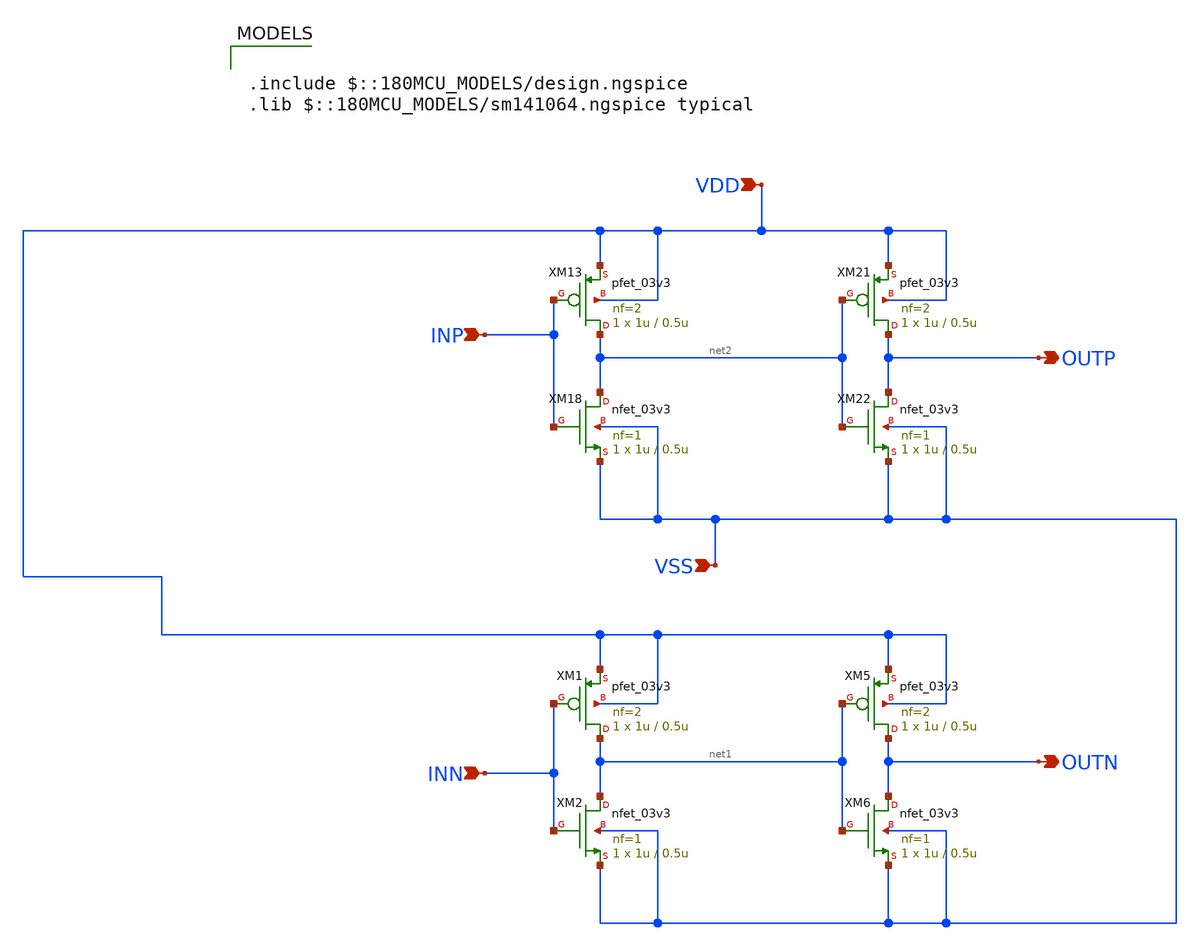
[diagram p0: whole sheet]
** sch_path: ISSCC26/submitted_notebooks/Low Mismatch 4 Channels Instrumentation Amplifier/Complementary Clock and Inverter/Schematic/clk_lpf_rev.sch
**.subckt clk_lpf_rev OUTP OUTN VDD VSS INP INN
*.opin OUTP
*.opin OUTN
*.ipin VDD
*.ipin VSS
*.ipin INP
*.ipin INN
XM1 net1 INN VDD VDD pfet_03v3 L=0.5u W=1u nf=2 ad='int((nf+1)/2) * W/nf * 0.18u' as='int((nf+2)/2) * W/nf * 0.18u'
+ pd='2*int((nf+1)/2) * (W/nf + 0.18u)' ps='2*int((nf+2)/2) * (W/nf + 0.18u)' nrd='0.18u / W' nrs='0.18u / W'
+ sa=0 sb=0 sd=0 m=1
XM2 net1 INN VSS VSS nfet_03v3 L=0.5u W=1u nf=1 ad='int((nf+1)/2) * W/nf * 0.18u' as='int((nf+2)/2) * W/nf * 0.18u'
+ pd='2*int((nf+1)/2) * (W/nf + 0.18u)' ps='2*int((nf+2)/2) * (W/nf + 0.18u)' nrd='0.18u / W' nrs='0.18u / W'
+ sa=0 sb=0 sd=0 m=1
XM5 OUTN net1 VDD VDD pfet_03v3 L=0.5u W=1u nf=2 ad='int((nf+1)/2) * W/nf * 0.18u' as='int((nf+2)/2) * W/nf * 0.18u'
+ pd='2*int((nf+1)/2) * (W/nf + 0.18u)' ps='2*int((nf+2)/2) * (W/nf + 0.18u)' nrd='0.18u / W' nrs='0.18u / W'
+ sa=0 sb=0 sd=0 m=1
XM6 OUTN net1 VSS VSS nfet_03v3 L=0.5u W=1u nf=1 ad='int((nf+1)/2) * W/nf * 0.18u' as='int((nf+2)/2) * W/nf * 0.18u'
+ pd='2*int((nf+1)/2) * (W/nf + 0.18u)' ps='2*int((nf+2)/2) * (W/nf + 0.18u)' nrd='0.18u / W' nrs='0.18u / W'
+ sa=0 sb=0 sd=0 m=1
XM13 net2 INP VDD VDD pfet_03v3 L=0.5u W=1u nf=2 ad='int((nf+1)/2) * W/nf * 0.18u' as='int((nf+2)/2) * W/nf * 0.18u'
+ pd='2*int((nf+1)/2) * (W/nf + 0.18u)' ps='2*int((nf+2)/2) * (W/nf + 0.18u)' nrd='0.18u / W' nrs='0.18u / W'
+ sa=0 sb=0 sd=0 m=1
XM18 net2 INP VSS VSS nfet_03v3 L=0.5u W=1u nf=1 ad='int((nf+1)/2) * W/nf * 0.18u' as='int((nf+2)/2) * W/nf * 0.18u'
+ pd='2*int((nf+1)/2) * (W/nf + 0.18u)' ps='2*int((nf+2)/2) * (W/nf + 0.18u)' nrd='0.18u / W' nrs='0.18u / W'
+ sa=0 sb=0 sd=0 m=1
XM21 OUTP net2 VDD VDD pfet_03v3 L=0.5u W=1u nf=2 ad='int((nf+1)/2) * W/nf * 0.18u' as='int((nf+2)/2) * W/nf * 0.18u'
+ pd='2*int((nf+1)/2) * (W/nf + 0.18u)' ps='2*int((nf+2)/2) * (W/nf + 0.18u)' nrd='0.18u / W' nrs='0.18u / W'
+ sa=0 sb=0 sd=0 m=1
XM22 OUTP net2 VSS VSS nfet_03v3 L=0.5u W=1u nf=1 ad='int((nf+1)/2) * W/nf * 0.18u' as='int((nf+2)/2) * W/nf * 0.18u'
+ pd='2*int((nf+1)/2) * (W/nf + 0.18u)' ps='2*int((nf+2)/2) * (W/nf + 0.18u)' nrd='0.18u / W' nrs='0.18u / W'
+ sa=0 sb=0 sd=0 m=1
**** begin user architecture code

.include $::180MCU_MODELS/design.ngspice
.lib $::180MCU_MODELS/sm141064.ngspice typical

**** end user architecture code
**.ends
.end
